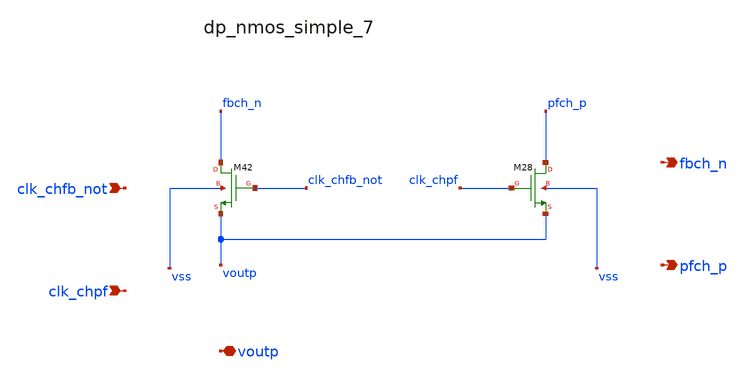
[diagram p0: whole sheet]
** sch_path: analog-db/raw/ia_003_fan_chopper_pf/hier/blocks/dp_nmos_simple_7.sch
**.subckt dp_nmos_simple_7 clk_chfb_not clk_chpf voutp fbch_n pfch_p
*.ipin clk_chfb_not
*.ipin clk_chpf
*.iopin voutp
*.opin fbch_n
*.opin pfch_p
XM28 pfch_p clk_chpf voutp vss sg13_lv_nmos w=x_dut_xm28_w l=x_dut_xm28_l ng=1 m=x_dut_xm28_m
XM42 fbch_n clk_chfb_not voutp vss sg13_lv_nmos w=x_dut_xm42_w l=x_dut_xm42_l ng=1 m=x_dut_xm42_m
**.ends
.end
